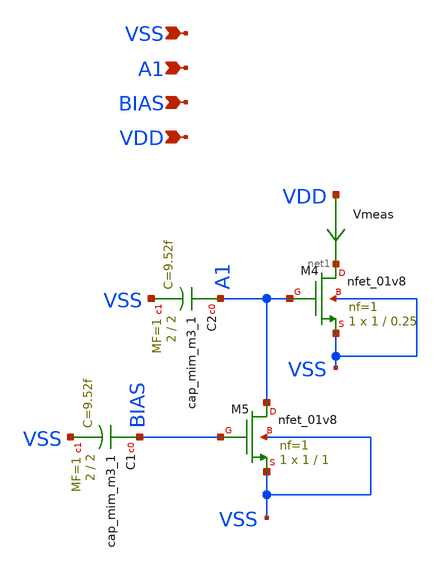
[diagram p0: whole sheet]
** sch_path: sch/transistor_evaluate_cap_0410.sch
**.subckt transistor_evaluate_cap_0410 VDD VSS BIAS A1
*.ipin VDD
*.ipin VSS
*.ipin BIAS
*.ipin A1
XM4 net1 A1 VSS VSS sky130_fd_pr__nfet_01v8 L=0.25 W=1 nf=1 ad='int((1 + 1)/2) * 1 / 1 * 0.29' as='int((1 + 2)/2) * 1 / 1 * 0.29'
+ pd='2*int((1 + 1)/2) * (1 / 1 + 0.29)' ps='2*int((1 + 2)/2) * (1 / 1 + 0.29)' nrd='0.29 / 1 ' nrs='0.29 / 1 '
+ sa=0 sb=0 sd=0 mult=1 m=1
XM5 A1 BIAS VSS VSS sky130_fd_pr__nfet_01v8 L=1 W=1 nf=1 ad='int((1 + 1)/2) * 1 / 1 * 0.29' as='int((1 + 2)/2) * 1 / 1 * 0.29'
+ pd='2*int((1 + 1)/2) * (1 / 1 + 0.29)' ps='2*int((1 + 2)/2) * (1 / 1 + 0.29)' nrd='0.29 / 1 ' nrs='0.29 / 1 '
+ sa=0 sb=0 sd=0 mult=1 m=1
XC1 BIAS VSS sky130_fd_pr__cap_mim_m3_1 W=2 L=2 MF=1 m=1
XC2 A1 VSS sky130_fd_pr__cap_mim_m3_1 W=2 L=2 MF=1 m=1
Vmeas VDD net1 0
.save i(vmeas)
**.ends
.end
